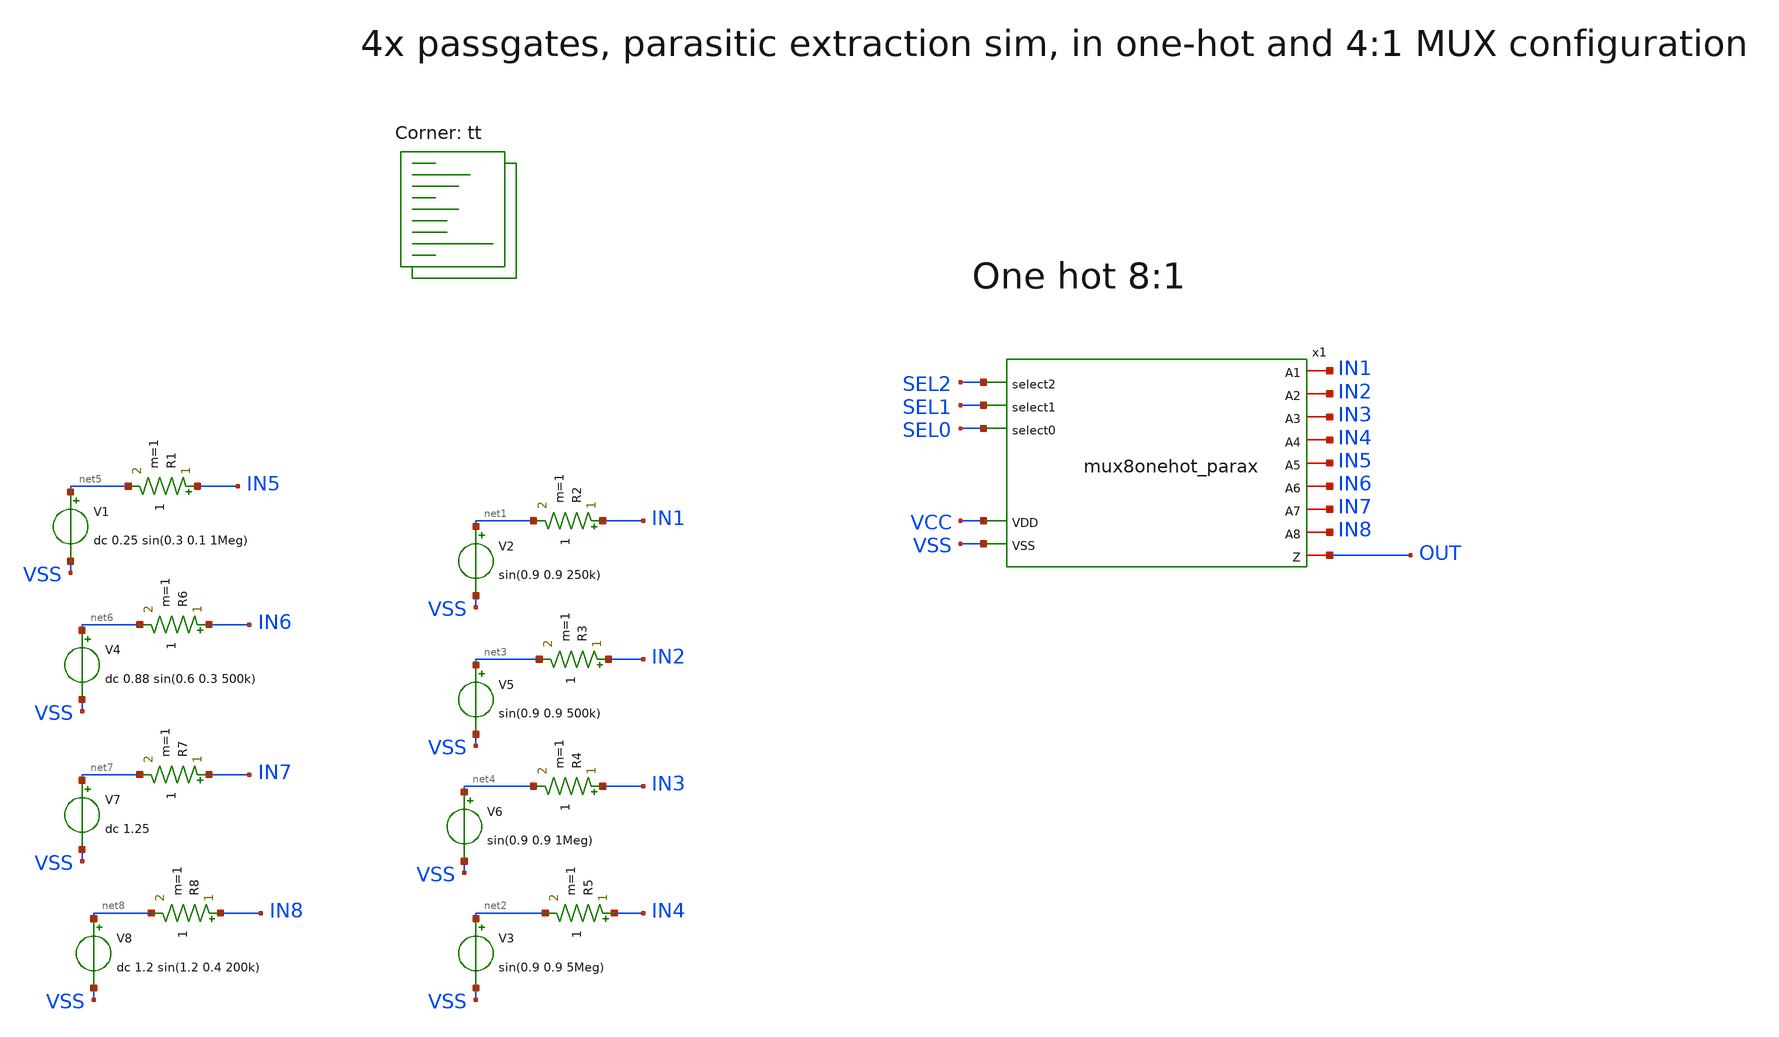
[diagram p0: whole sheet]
** sch_path: xschem/tb_8muxonehot.sch
**.subckt tb_8muxonehot
V2 net1 VSS sin(0.9 0.9 250k)
V3 net2 VSS sin(0.9 0.9 5Meg)
V5 net3 VSS sin(0.9 0.9 500k)
V6 net4 VSS sin(0.9 0.9 1Meg)
R2 IN1 net1 1 m=1
R3 IN2 net3 1 m=1
R4 IN3 net4 1 m=1
R5 IN4 net2 1 m=1
x1 VCC VSS SEL0 SEL1 IN1 IN5 IN6 IN2 IN7 IN3 SEL2 IN8 IN4 OUT mux8onehot_parax
V1 net5 VSS dc 0.25 sin(0.3 0.1 1Meg)
R1 IN5 net5 1 m=1
V4 net6 VSS dc 0.88 sin(0.6 0.3 500k)
R6 IN6 net6 1 m=1
V7 net7 VSS dc 1.25
R7 IN7 net7 1 m=1
V8 net8 VSS dc 1.2 sin(1.2 0.4 200k)
R8 IN8 net8 1 m=1
**** begin user architecture code
.lib $::SKYWATER_MODELS/sky130.lib.spice tt
**** end user architecture code
**.ends

* expanding   symbol:  /home/ttuser/vmswap/tt09-analogmux/xschem/mux8onehot_parax.sym # of pins=14
** sym_path: xschem/mux8onehot.sym
.include [file normalize extracted/mux8onehot_parax.spice]
**** begin user architecture code


* ngspice commands
* .options savecurrents
.param VCC = 1.8
.param SRCRES = 1k
.include stimuli_tb_8muxonehot.cir
.control
save all
op
write tb_8muxonehot.raw
set appendwrite
tran 200n 120u
write tb_8muxonehot.raw
quit 0
.endc



**** end user architecture code
.end
